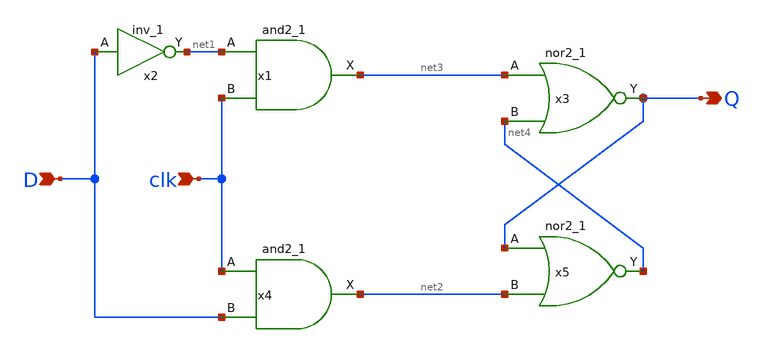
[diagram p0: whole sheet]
** sch_path: xschem/comparator/latchnorandinv.sch
**.subckt latchnorandinv D clk Q
*.ipin D
*.ipin clk
*.opin Q
x1 net1 clk GND GND VDD VDD net3 sky130_fd_sc_lp__and2_1
x2 D GND GND VDD VDD net1 sky130_fd_sc_lp__inv_1
x3 net3 net4 GND GND VDD VDD Q sky130_fd_sc_lp__nor2_1
x4 clk D GND GND VDD VDD net2 sky130_fd_sc_lp__and2_1
x5 Q net2 GND GND VDD VDD net4 sky130_fd_sc_lp__nor2_1
**.ends
.end
